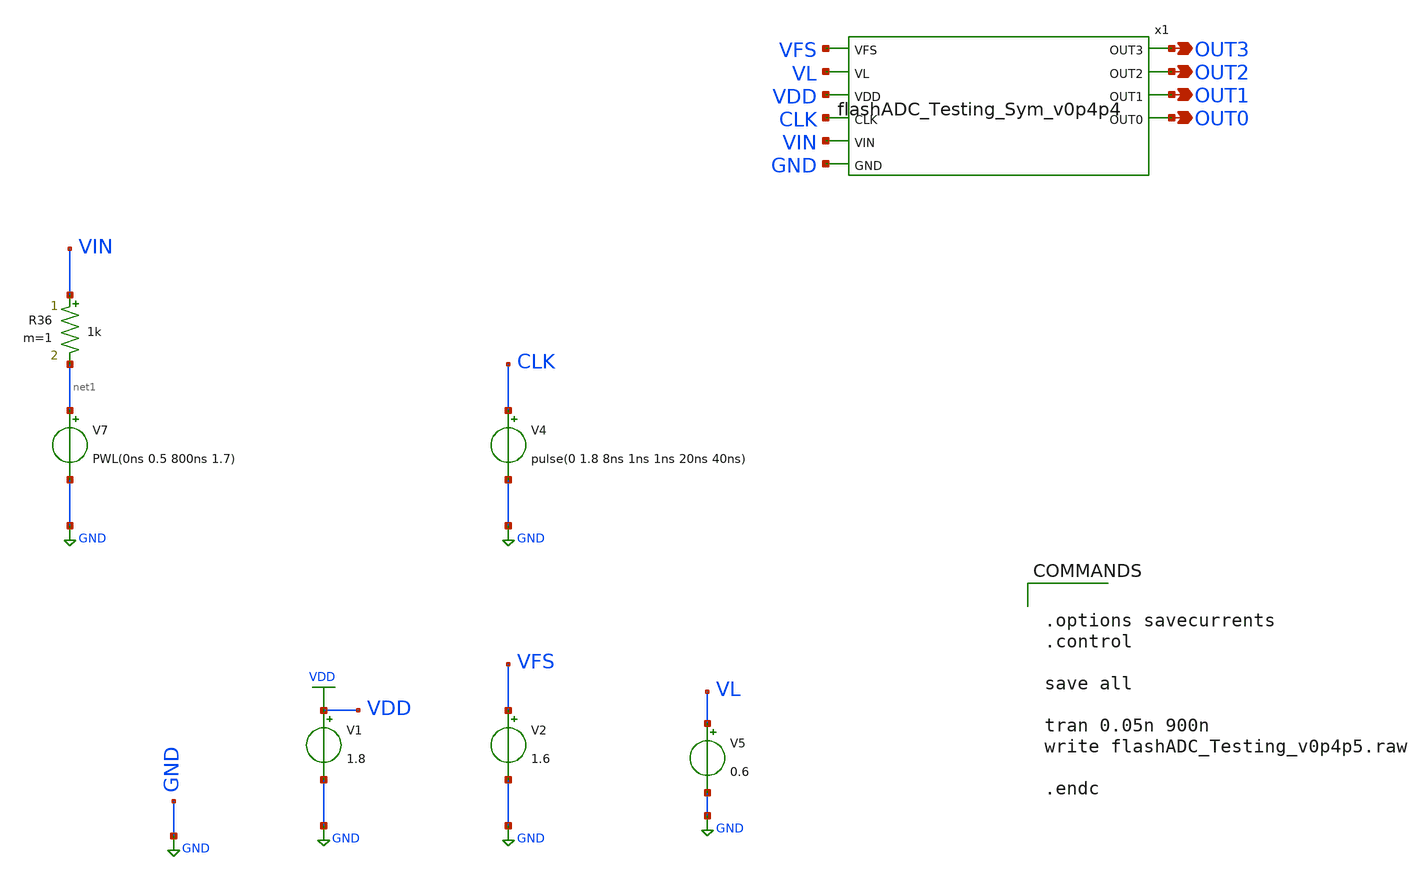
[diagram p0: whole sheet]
** sch_path: flashADC/xschem/flashADC_Testing_v0p4p5.sch
.lib $::SKYWATER_MODELS/sky130.lib.spice tt
.include $::SKYWATER_STDCELLS/sky130_fd_sc_hd.spice

**.subckt flashADC_Testing_v0p4p5 OUT3 OUT2 OUT1 OUT0
*.opin OUT3
*.opin OUT2
*.opin OUT1
*.opin OUT0
V4 CLK GND pulse(0 1.8 8ns 1ns 1ns 20ns 40ns)
V1 VDD GND 1.8
V2 VFS GND 1.6
V5 VL GND 0.6
V7 net1 GND PWL(0ns 0.5 800ns 1.7)
R36 VIN net1 1k m=1
x1 VFS OUT3 OUT2 OUT1 OUT0 VL VDD CLK VIN GND flashADC_Testing_Sym_v0p4p4
**** begin user architecture code


.options savecurrents
.control

save all

tran 0.05n 900n
write flashADC_Testing_v0p4p5.raw

.endc


**** end user architecture code
**.ends
.GLOBAL GND
.GLOBAL VDD
.end
